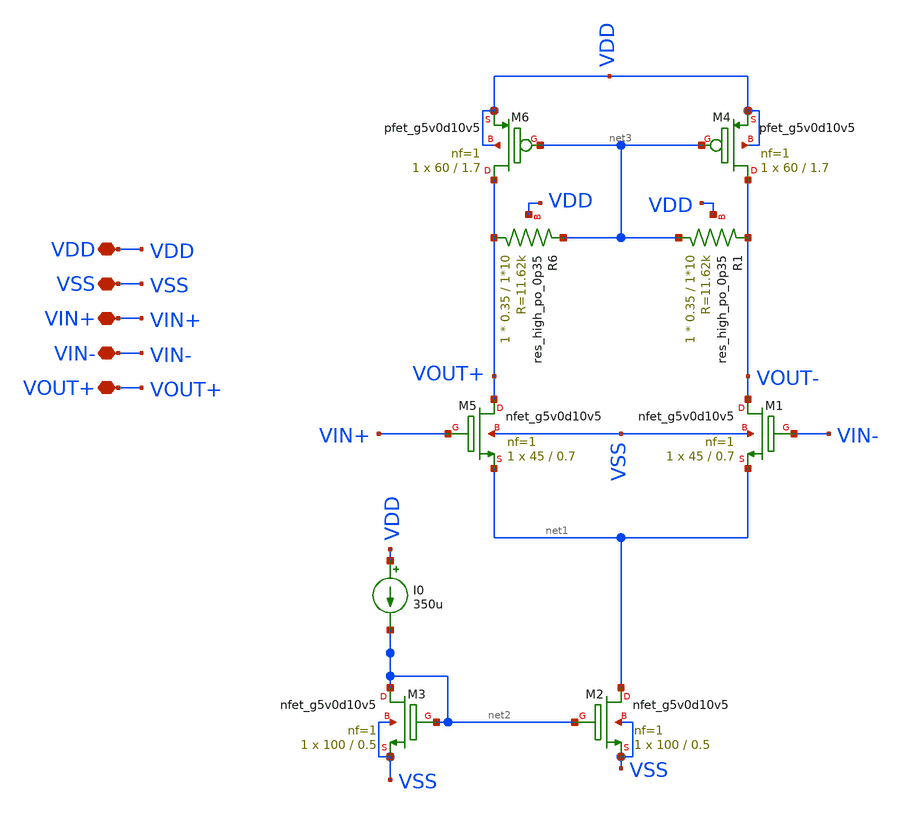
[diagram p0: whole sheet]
** sch_path: old stuff/amplifiers/differencial_stage_amps/stange stages/diode_feedback/differential_stage.sch
**.subckt differential_stage VDD VSS VIN+ VIN- VOUT+
*.iopin VDD
*.iopin VSS
*.iopin VIN+
*.iopin VIN-
*.iopin VOUT+
XM5 VOUT+ VIN+ net1 VSS sky130_fd_pr__nfet_g5v0d10v5 L=0.7 W=45 nf=1 ad='int((1 + 1)/2) * 45 / 1 * 0.29'
+ as='int((1 + 2)/2) * 45 / 1 * 0.29' pd='2*int((1 + 1)/2) * (45 / 1 + 0.29)' ps='2*int((1 + 2)/2) * (45 / 1 + 0.29)'
+ nrd='0.29 / 45 ' nrs='0.29 / 45 ' sa=0 sb=0 sd=0 mult=1 m=1
XM1 VOUT- VIN- net1 VSS sky130_fd_pr__nfet_g5v0d10v5 L=0.7 W=45 nf=1 ad='int((1 + 1)/2) * 45 / 1 * 0.29'
+ as='int((1 + 2)/2) * 45 / 1 * 0.29' pd='2*int((1 + 1)/2) * (45 / 1 + 0.29)' ps='2*int((1 + 2)/2) * (45 / 1 + 0.29)'
+ nrd='0.29 / 45 ' nrs='0.29 / 45 ' sa=0 sb=0 sd=0 mult=1 m=1
XM2 net1 net2 VSS VSS sky130_fd_pr__nfet_g5v0d10v5 L=0.5 W=100 nf=1 ad='int((1 + 1)/2) * 100 / 1 * 0.29'
+ as='int((1 + 2)/2) * 100 / 1 * 0.29' pd='2*int((1 + 1)/2) * (100 / 1 + 0.29)' ps='2*int((1 + 2)/2) * (100 / 1 + 0.29)'
+ nrd='0.29 / 100 ' nrs='0.29 / 100 ' sa=0 sb=0 sd=0 mult=1 m=1
XM3 net2 net2 VSS VSS sky130_fd_pr__nfet_g5v0d10v5 L=0.5 W=100 nf=1 ad='int((1 + 1)/2) * 100 / 1 * 0.29'
+ as='int((1 + 2)/2) * 100 / 1 * 0.29' pd='2*int((1 + 1)/2) * (100 / 1 + 0.29)' ps='2*int((1 + 2)/2) * (100 / 1 + 0.29)'
+ nrd='0.29 / 100 ' nrs='0.29 / 100 ' sa=0 sb=0 sd=0 mult=1 m=1
I0 VDD net2 350u
XM4 VOUT- net3 VDD VDD sky130_fd_pr__pfet_g5v0d10v5 L=1.7 W=60 nf=1 ad='int((1 + 1)/2) * 60 / 1 * 0.29'
+ as='int((1 + 2)/2) * 60 / 1 * 0.29' pd='2*int((1 + 1)/2) * (60 / 1 + 0.29)' ps='2*int((1 + 2)/2) * (60 / 1 + 0.29)'
+ nrd='0.29 / 60 ' nrs='0.29 / 60 ' sa=0 sb=0 sd=0 mult=1 m=1
XM6 VOUT+ net3 VDD VDD sky130_fd_pr__pfet_g5v0d10v5 L=1.7 W=60 nf=1 ad='int((1 + 1)/2) * 60 / 1 * 0.29'
+ as='int((1 + 2)/2) * 60 / 1 * 0.29' pd='2*int((1 + 1)/2) * (60 / 1 + 0.29)' ps='2*int((1 + 2)/2) * (60 / 1 + 0.29)'
+ nrd='0.29 / 60 ' nrs='0.29 / 60 ' sa=0 sb=0 sd=0 mult=1 m=1
XR6 VOUT+ net3 VDD sky130_fd_pr__res_high_po_0p35 L=1*10 mult=1 m=1
XR1 net3 VOUT- VDD sky130_fd_pr__res_high_po_0p35 L=1*10 mult=1 m=1
**.ends
.end
